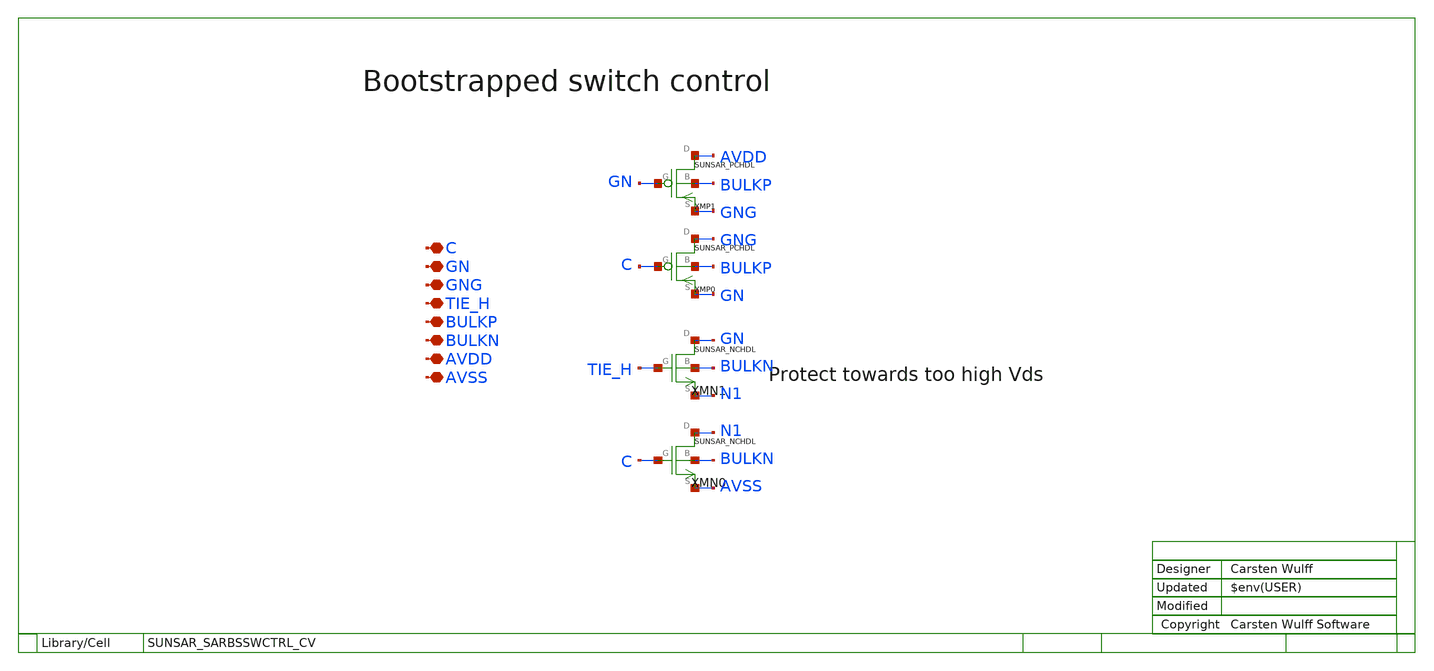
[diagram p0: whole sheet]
** sch_path: ip/sun_sar9b_sky130nm/design/SUN_SAR9B_SKY130NM/SUNSAR_SARBSSWCTRL_CV.sch
**.subckt SUNSAR_SARBSSWCTRL_CV C GN GNG TIE_H BULKP BULKN AVDD AVSS
*.iopin C
*.iopin GN
*.iopin GNG
*.iopin TIE_H
*.iopin BULKP
*.iopin BULKN
*.iopin AVDD
*.iopin AVSS
XMN0 N1 C AVSS BULKN SUNSAR_NCHDL
XMN1 GN TIE_H N1 BULKN SUNSAR_NCHDL
XMP0 GNG C GN BULKP SUNSAR_PCHDL
XMP1 AVDD GN GNG BULKP SUNSAR_PCHDL
**.ends
.end
